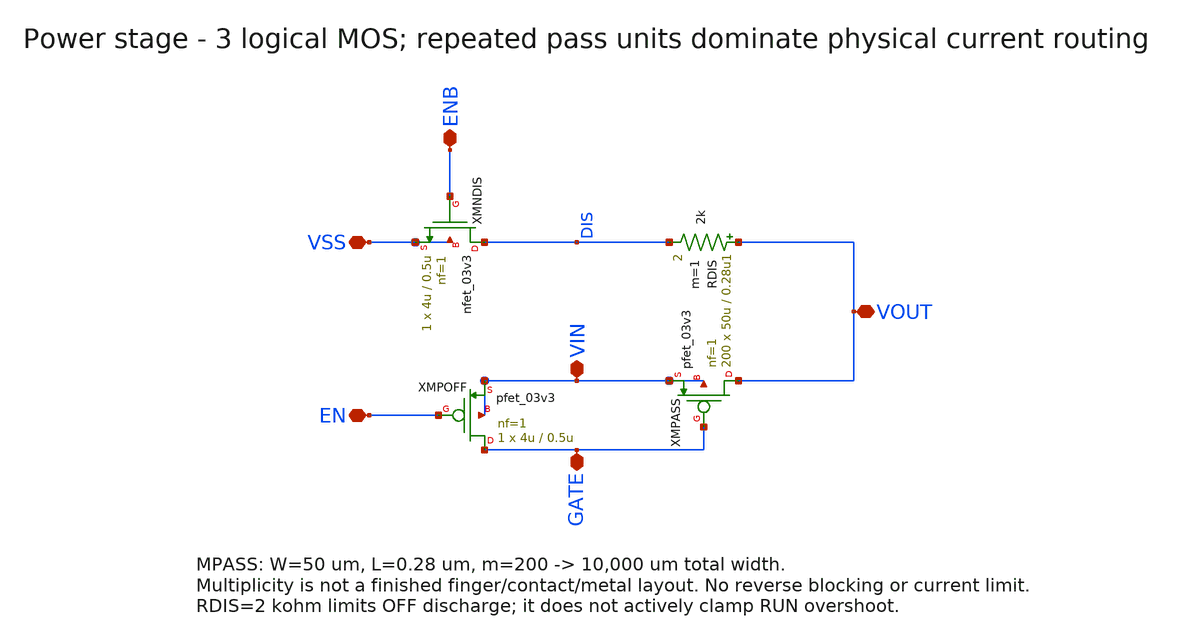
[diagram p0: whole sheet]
** sch_path: schematics/ldo_power_stage.sch
**.subckt ldo_power_stage VIN VSS EN ENB GATE VOUT
*.iopin VIN
*.iopin VSS
*.iopin EN
*.iopin ENB
*.iopin GATE
*.iopin VOUT
XMPASS VOUT GATE VIN VIN pfet_03v3 L=0.28u W=50u nf=1 ad='int((nf+1)/2)*W/nf*0.18u' as='int((nf+2)/2)*W/nf*0.18u'
+ pd='2*int((nf+1)/2)*(W/nf+0.18u)' ps='2*int((nf+2)/2)*(W/nf+0.18u)' nrd='0.18u/W' nrs='0.18u/W' sa=0
+ sb=0 sd=0 m=200 par=200
XMPOFF GATE EN VIN VIN pfet_03v3 L=0.5u W=4u nf=1 ad='int((nf+1)/2)*W/nf*0.18u' as='int((nf+2)/2)*W/nf*0.18u'
+ pd='2*int((nf+1)/2)*(W/nf+0.18u)' ps='2*int((nf+2)/2)*(W/nf+0.18u)' nrd='0.18u/W' nrs='0.18u/W' sa=0
+ sb=0 sd=0 m=1 par=1
RDIS VOUT DIS 2k m=1
XMNDIS DIS ENB VSS VSS nfet_03v3 L=0.5u W=4u nf=1 ad='int((nf+1)/2)*W/nf*0.18u' as='int((nf+2)/2)*W/nf*0.18u'
+ pd='2*int((nf+1)/2)*(W/nf+0.18u)' ps='2*int((nf+2)/2)*(W/nf+0.18u)' nrd='0.18u/W' nrs='0.18u/W' sa=0
+ sb=0 sd=0 m=1 par=1
**.ends
.end
